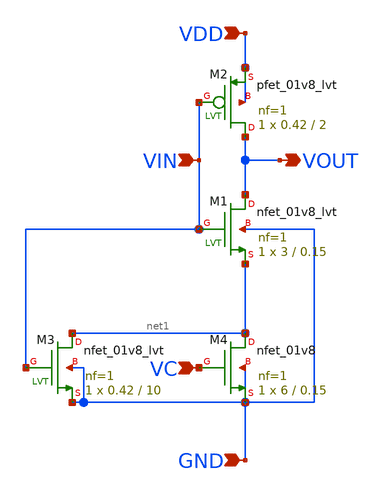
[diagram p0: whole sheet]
** sch_path: design/LELO_SVOD_SKY130A/LELO_RING_DEL_VC_FAST.sch
**.subckt LELO_RING_DEL_VC_FAST VIN VDD VOUT VC GND
*.ipin VIN
*.ipin VDD
*.opin VOUT
*.ipin VC
*.ipin GND
XM1 VOUT VIN net1 GND sky130_fd_pr__nfet_01v8_lvt L=0.15 W=3 nf=1 ad='int((1 + 1)/2) * 3 / 1 * 0.29'
+ as='int((1 + 2)/2) * 3 / 1 * 0.29' pd='2*int((1 + 1)/2) * (3 / 1 + 0.29)' ps='2*int((1 + 2)/2) * (3 / 1 + 0.29)'
+ nrd='0.29 / 3 ' nrs='0.29 / 3 ' sa=0 sb=0 sd=0 mult=1 m=1
XM2 VOUT VIN VDD VDD sky130_fd_pr__pfet_01v8_lvt L=2 W=0.42 nf=1 ad='int((1 + 1)/2) * 0.42 / 1 * 0.29'
+ as='int((1 + 2)/2) * 0.42 / 1 * 0.29' pd='2*int((1 + 1)/2) * (0.42 / 1 + 0.29)' ps='2*int((1 + 2)/2) * (0.42 / 1 + 0.29)'
+ nrd='0.29 / 0.42 ' nrs='0.29 / 0.42 ' sa=0 sb=0 sd=0 mult=1 m=1
XM3 net1 VIN GND GND sky130_fd_pr__nfet_01v8_lvt L=10 W=0.42 nf=1 ad='int((1 + 1)/2) * 0.42 / 1 * 0.29'
+ as='int((1 + 2)/2) * 0.42 / 1 * 0.29' pd='2*int((1 + 1)/2) * (0.42 / 1 + 0.29)' ps='2*int((1 + 2)/2) * (0.42 / 1 + 0.29)'
+ nrd='0.29 / 0.42 ' nrs='0.29 / 0.42 ' sa=0 sb=0 sd=0 mult=1 m=1
XM4 net1 VC GND GND sky130_fd_pr__nfet_01v8 L=0.15 W=6 nf=1 ad='int((1 + 1)/2) * 6 / 1 * 0.29' as='int((1 + 2)/2) * 6 / 1 * 0.29'
+ pd='2*int((1 + 1)/2) * (6 / 1 + 0.29)' ps='2*int((1 + 2)/2) * (6 / 1 + 0.29)' nrd='0.29 / 6 ' nrs='0.29 / 6 '
+ sa=0 sb=0 sd=0 mult=1 m=1
**.ends
.end
